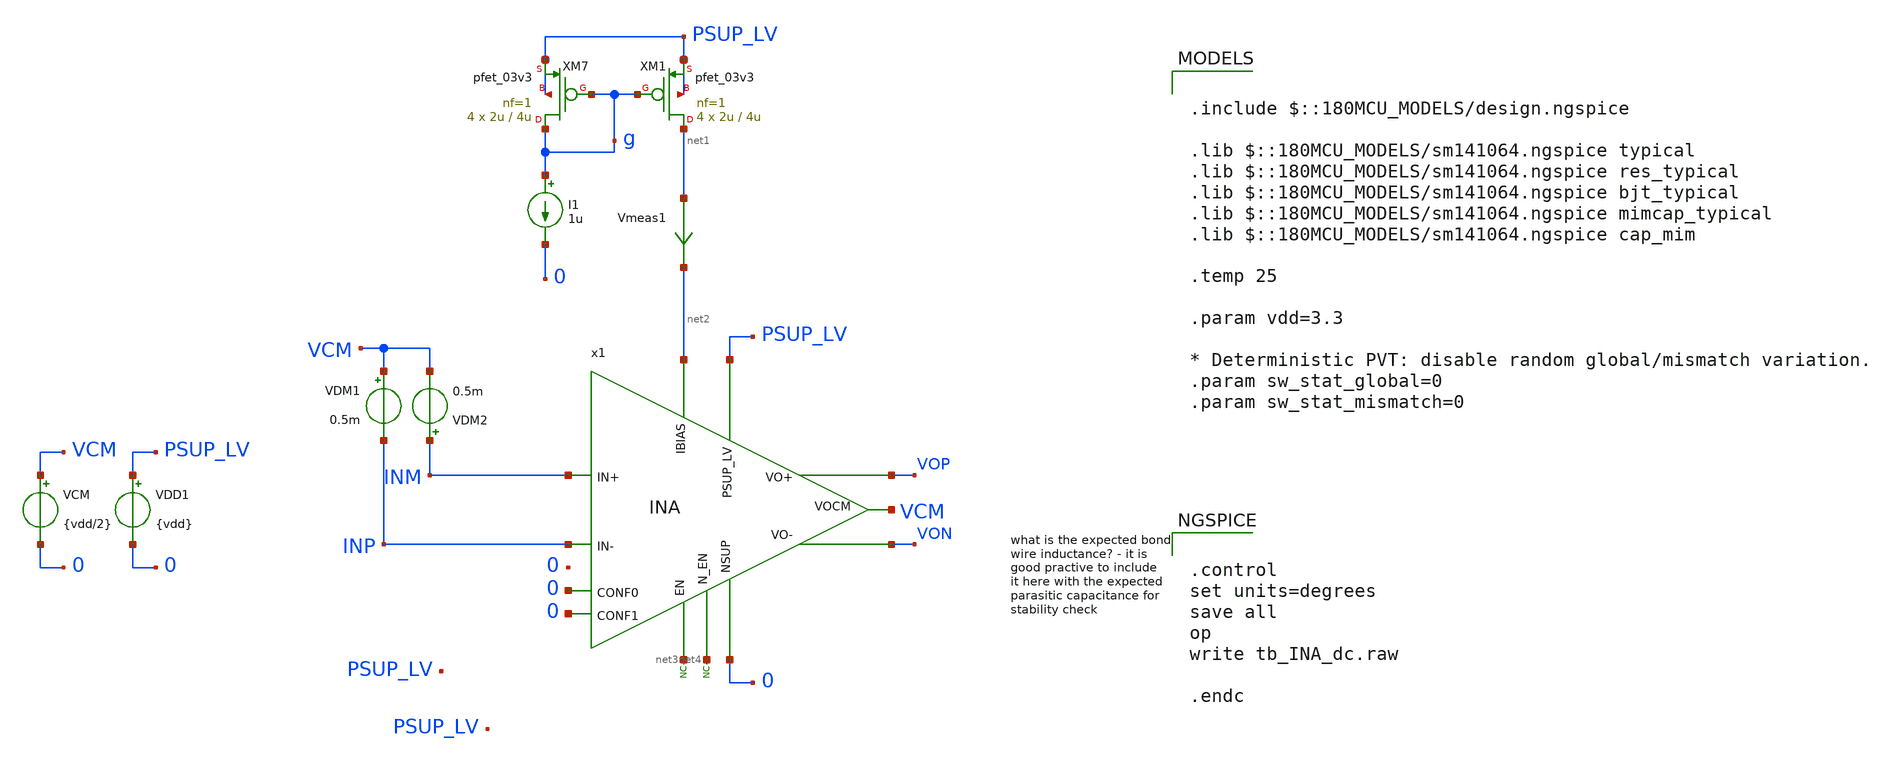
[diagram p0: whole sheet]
** sch_path: xschem/blocks/INA/tb_INA_dc.sch
**.subckt tb_INA_dc
VDD1 PSUP_LV 0 {vdd}
VCM VCM 0 {vdd/2}
* noconn #net3
* noconn #net4
VDM2 INM VCM 0.5m
VDM1 VCM INP 0.5m
x1 PSUP_LV 0 net3 net4 net2 0 0 INM VOP VCM INP VON INA
XM7 g g PSUP_LV PSUP_LV pfet_03v3 L=4u W=2u nf=1 ad='int((nf+1)/2) * W/nf * 0.18u' as='int((nf+2)/2) * W/nf * 0.18u'
+ pd='2*int((nf+1)/2) * (W/nf + 0.18u)' ps='2*int((nf+2)/2) * (W/nf + 0.18u)' nrd='0.18u / W' nrs='0.18u / W'
+ sa=0 sb=0 sd=0 m=4
XM1 net1 g PSUP_LV PSUP_LV pfet_03v3 L=4u W=2u nf=1 ad='int((nf+1)/2) * W/nf * 0.18u' as='int((nf+2)/2) * W/nf * 0.18u'
+ pd='2*int((nf+1)/2) * (W/nf + 0.18u)' ps='2*int((nf+2)/2) * (W/nf + 0.18u)' nrd='0.18u / W' nrs='0.18u / W'
+ sa=0 sb=0 sd=0 m=4
I1 g 0 1u
Vmeas1 net1 net2 0
.save i(vmeas1)
**** begin user architecture code

.include $::180MCU_MODELS/design.ngspice

.lib $::180MCU_MODELS/sm141064.ngspice typical
.lib $::180MCU_MODELS/sm141064.ngspice res_typical
.lib $::180MCU_MODELS/sm141064.ngspice bjt_typical
.lib $::180MCU_MODELS/sm141064.ngspice mimcap_typical
.lib $::180MCU_MODELS/sm141064.ngspice cap_mim

.temp 25

.param vdd=3.3

* Deterministic PVT: disable random global/mismatch variation.
.param sw_stat_global=0
.param sw_stat_mismatch=0



.control
set units=degrees
save all
op
write tb_INA_dc.raw

.endc


**** end user architecture code
**.ends
.end
